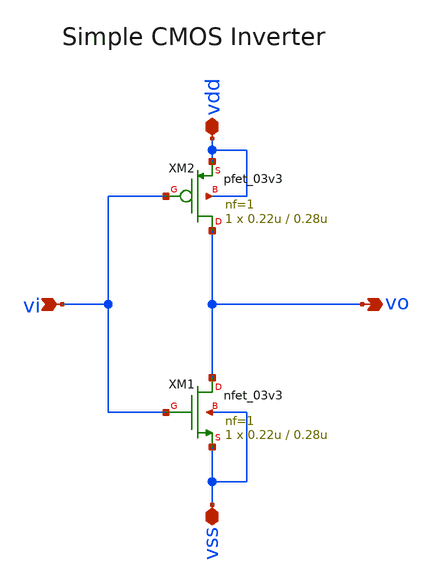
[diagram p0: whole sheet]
** sch_path: designs/sar_adc/comparator/xschem/comparador/xschem/Inverter/inv.sch
**.subckt inv vdd vss vi vo
*.iopin vdd
*.iopin vss
*.ipin vi
*.opin vo
XM1 vo vi vss vss nfet_03v3 L=0.28u W=0.22u nf=1 ad='int((nf+1)/2) * W/nf * 0.18u' as='int((nf+2)/2) * W/nf * 0.18u'
+ pd='2*int((nf+1)/2) * (W/nf + 0.18u)' ps='2*int((nf+2)/2) * (W/nf + 0.18u)' nrd='0.18u / W' nrs='0.18u / W'
+ sa=0 sb=0 sd=0 m=1
XM2 vo vi vdd vdd pfet_03v3 L=0.28u W=0.22u nf=1 ad='int((nf+1)/2) * W/nf * 0.18u' as='int((nf+2)/2) * W/nf * 0.18u'
+ pd='2*int((nf+1)/2) * (W/nf + 0.18u)' ps='2*int((nf+2)/2) * (W/nf + 0.18u)' nrd='0.18u / W' nrs='0.18u / W'
+ sa=0 sb=0 sd=0 m=1
**.ends
.end
